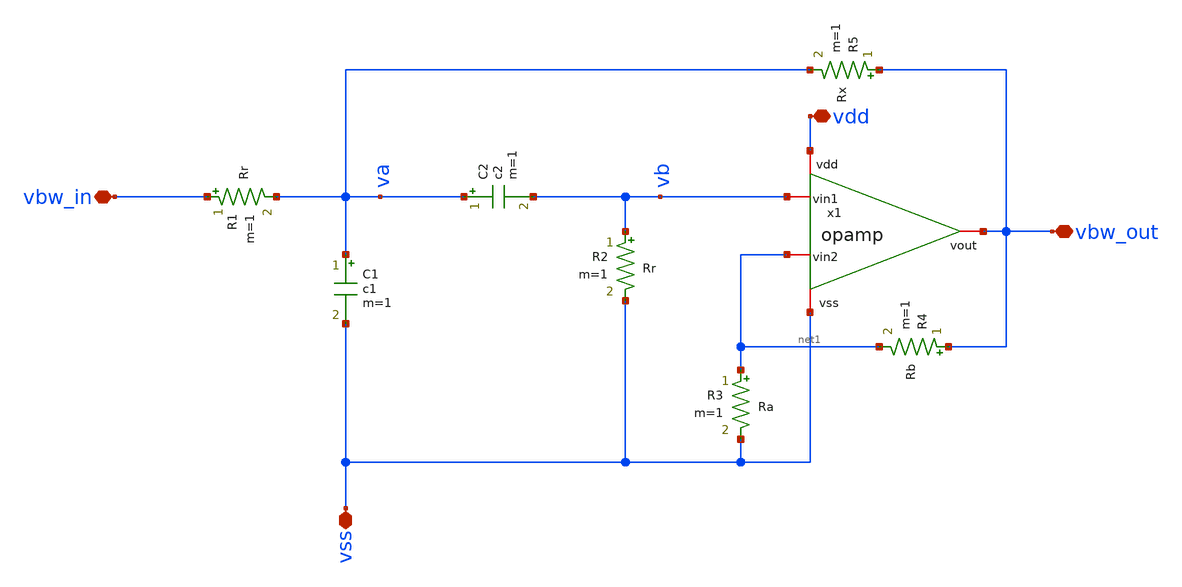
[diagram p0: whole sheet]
** sch_path: Synapse/bpfilter.sch
**.subckt bpfilter vbw_in vbw_out vdd vss
*.iopin vbw_in
*.iopin vbw_out
*.iopin vdd
*.iopin vss
R1 vbw_in va Rr m=1
R2 vb vss Rr m=1
C2 va vb c2 m=1
C1 va vss c1 m=1
x1 vdd vbw_out vb net1 vss opamp
R3 net1 vss Ra m=1
R4 vbw_out net1 Rb m=1
R5 vbw_out va Rx m=1
**.ends

* expanding   symbol:  /home/alex/Desktop/EDA/SNN_IPN/OPAMP/opamp.sym # of pins=5
** sym_path: OPAMP/opamp.sym
** sch_path: OPAMP/opamp.sch
.subckt opamp vdd vout vin1 vin2 vss
*.iopin vin2
*.iopin vin1
*.iopin vdd
*.iopin vss
*.iopin vout
XM1 net3 net3 vdd vdd sky130_fd_pr__pfet_01v8 L=0.15 W=2 nf=1 ad='int((nf+1)/2) * W/nf * 0.29' as='int((nf+2)/2) * W/nf * 0.29'
+ pd='2*int((nf+1)/2) * (W/nf + 0.29)' ps='2*int((nf+2)/2) * (W/nf + 0.29)' nrd='0.29 / W' nrs='0.29 / W'
+ sa=0 sb=0 sd=0 mult=1 m=1
XM2 vout net3 vdd vdd sky130_fd_pr__pfet_01v8 L=0.15 W=2 nf=1 ad='int((nf+1)/2) * W/nf * 0.29' as='int((nf+2)/2) * W/nf * 0.29'
+ pd='2*int((nf+1)/2) * (W/nf + 0.29)' ps='2*int((nf+2)/2) * (W/nf + 0.29)' nrd='0.29 / W' nrs='0.29 / W'
+ sa=0 sb=0 sd=0 mult=1 m=1
XM3 net3 vin1 net2 vss sky130_fd_pr__nfet_01v8 L=0.15 W=1 nf=1 ad='int((nf+1)/2) * W/nf * 0.29' as='int((nf+2)/2) * W/nf * 0.29'
+ pd='2*int((nf+1)/2) * (W/nf + 0.29)' ps='2*int((nf+2)/2) * (W/nf + 0.29)' nrd='0.29 / W' nrs='0.29 / W'
+ sa=0 sb=0 sd=0 mult=1 m=1
XM4 vout vin2 net2 vss sky130_fd_pr__nfet_01v8 L=0.15 W=1 nf=1 ad='int((nf+1)/2) * W/nf * 0.29' as='int((nf+2)/2) * W/nf * 0.29'
+ pd='2*int((nf+1)/2) * (W/nf + 0.29)' ps='2*int((nf+2)/2) * (W/nf + 0.29)' nrd='0.29 / W' nrs='0.29 / W'
+ sa=0 sb=0 sd=0 mult=1 m=1
XM5 net2 net1 vss vss sky130_fd_pr__nfet_01v8 L=0.15 W=1 nf=1 ad='int((nf+1)/2) * W/nf * 0.29' as='int((nf+2)/2) * W/nf * 0.29'
+ pd='2*int((nf+1)/2) * (W/nf + 0.29)' ps='2*int((nf+2)/2) * (W/nf + 0.29)' nrd='0.29 / W' nrs='0.29 / W'
+ sa=0 sb=0 sd=0 mult=1 m=1
XM6 net1 net1 vss vss sky130_fd_pr__nfet_01v8 L=0.15 W=1 nf=1 ad='int((nf+1)/2) * W/nf * 0.29' as='int((nf+2)/2) * W/nf * 0.29'
+ pd='2*int((nf+1)/2) * (W/nf + 0.29)' ps='2*int((nf+2)/2) * (W/nf + 0.29)' nrd='0.29 / W' nrs='0.29 / W'
+ sa=0 sb=0 sd=0 mult=1 m=1
R2 vdd net1 1k m=1
.ends

.end
